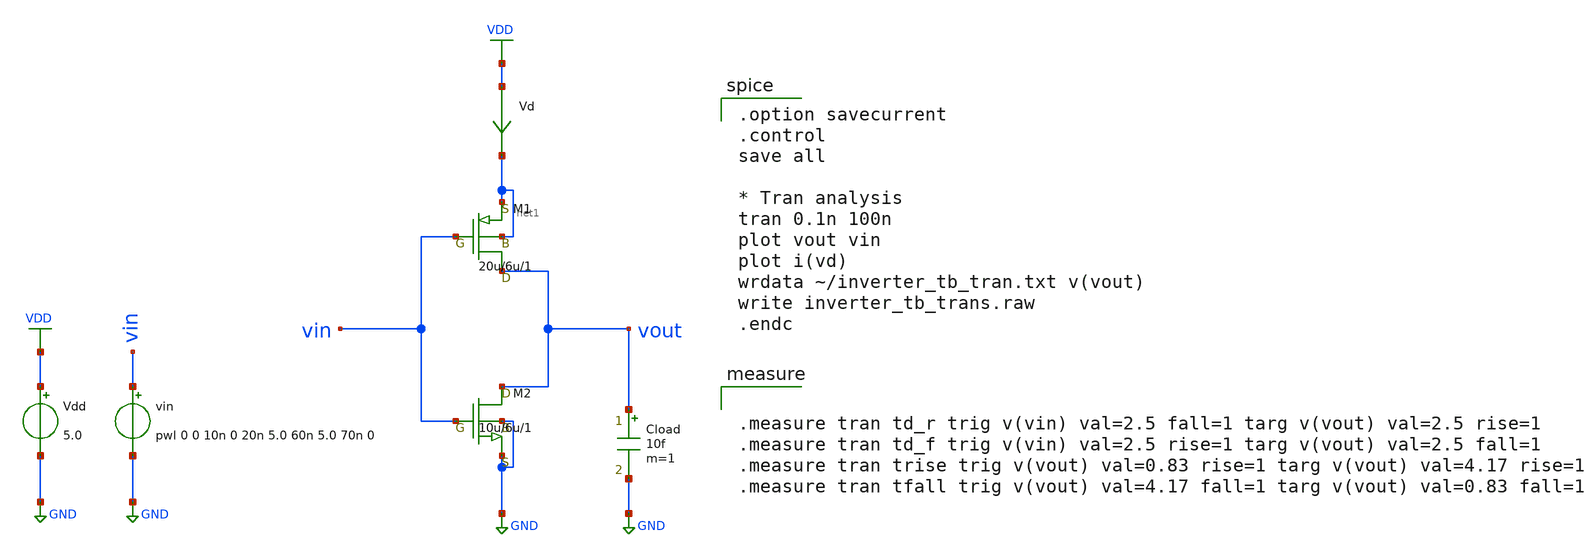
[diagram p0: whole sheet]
** sch_path: samples/inverter/MF20/inverter_tb_trans.sch
**.subckt inverter_tb_trans
Vdd VDD GND 5.0
vin vin GND pwl 0 0 10n 0 20n 5.0 60n 5.0 70n 0
Vd VDD net1 0
.save i(vd)
Cload vout GND 10f m=1
M1 vout vin net1 net1 pch w=20u l=6u as=0 ps=0 ad=0 pd=0 m=1
M2 vout vin GND GND nch w=10u l=6u as=0 ps=0 ad=0 pd=0 m=1
**** begin user architecture code

.option savecurrent
.control
save all

* Tran analysis
tran 0.1n 100n
plot vout vin
plot i(vd)
wrdata ~/inverter_tb_tran.txt v(vout)
write inverter_tb_trans.raw
.endc



.measure tran td_r trig v(vin) val=2.5 fall=1 targ v(vout) val=2.5 rise=1
.measure tran td_f trig v(vin) val=2.5 rise=1 targ v(vout) val=2.5 fall=1
.measure tran trise trig v(vout) val=0.83 rise=1 targ v(vout) val=4.17 rise=1
.measure tran tfall trig v(vout) val=4.17 fall=1 targ v(vout) val=0.83 fall=1


 .include $::LIB/SOI_CMOS
**** end user architecture code
**.ends
.GLOBAL VDD
.GLOBAL GND
.end
